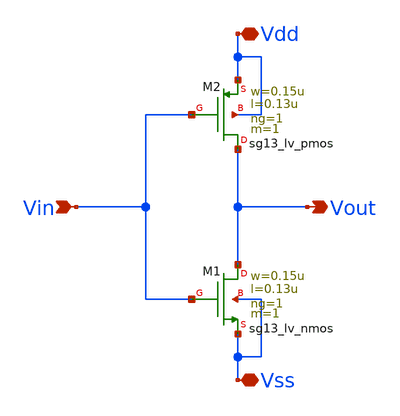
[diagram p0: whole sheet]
** sch_path: 4xPI/Pruebas/InversorMio.sch
**.subckt InversorMio Vss Vdd Vin Vout
*.iopin Vss
*.iopin Vdd
*.ipin Vin
*.opin Vout
XM1 Vout Vin Vss Vss sg13_lv_nmos w=0.15u l=0.13u ng=1 m=1 mm_ok=1
XM2 Vout Vin Vdd Vdd sg13_lv_pmos w=0.15u l=0.13u ng=1 m=1 mm_ok=1
**.ends
.end
